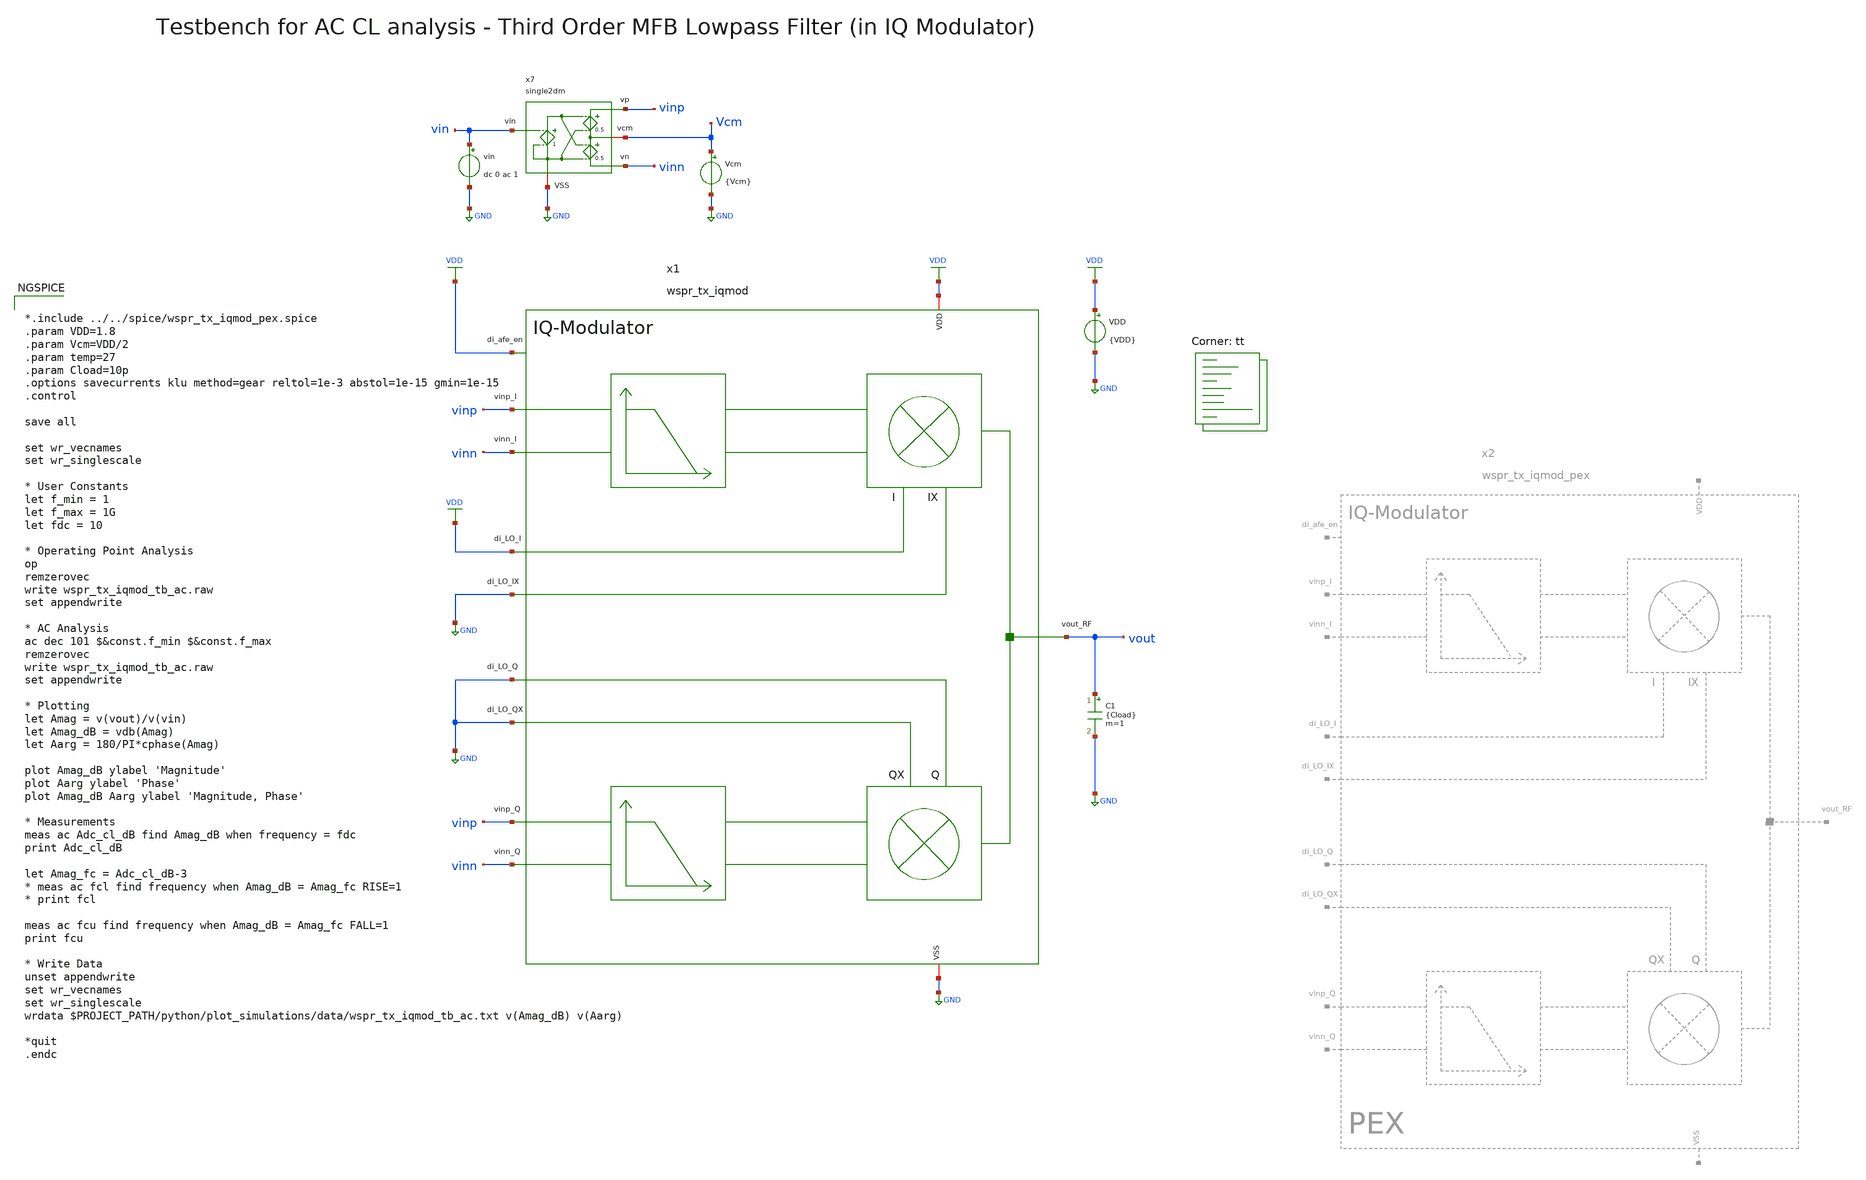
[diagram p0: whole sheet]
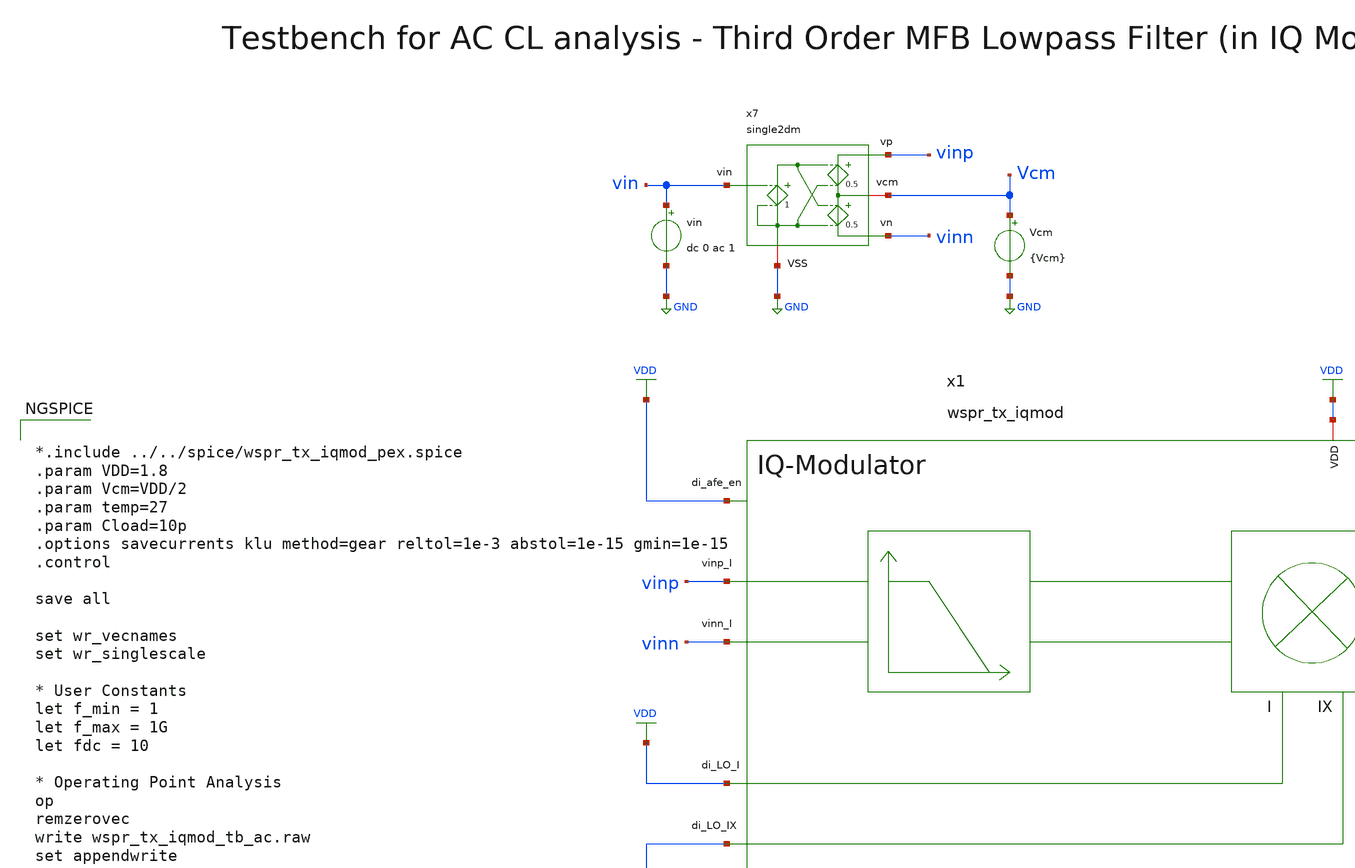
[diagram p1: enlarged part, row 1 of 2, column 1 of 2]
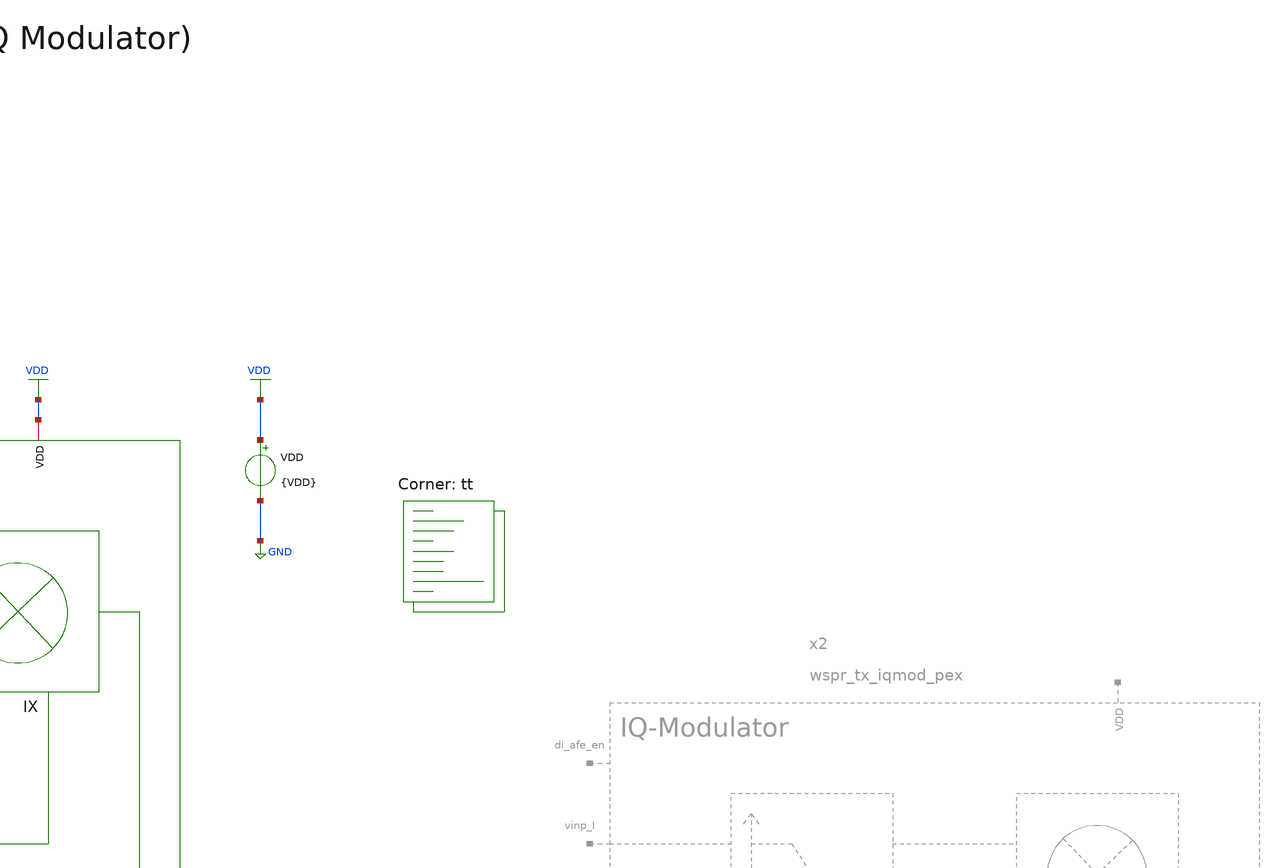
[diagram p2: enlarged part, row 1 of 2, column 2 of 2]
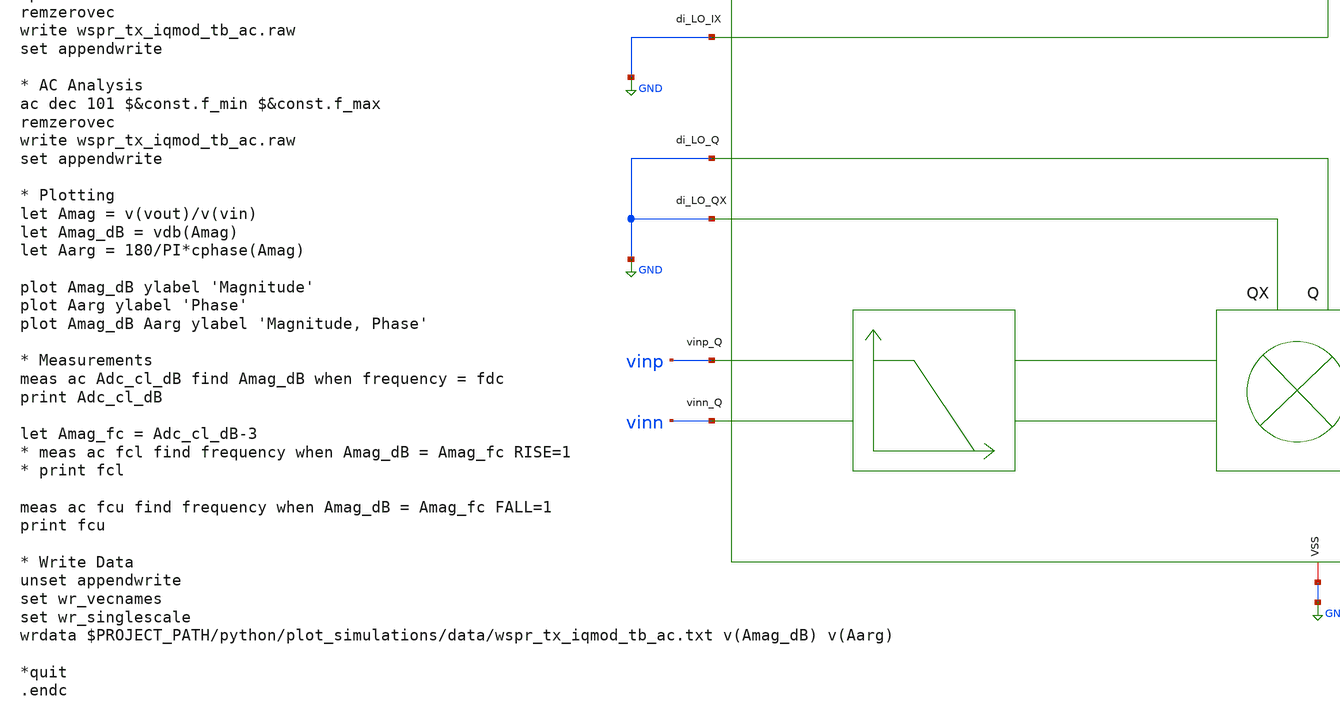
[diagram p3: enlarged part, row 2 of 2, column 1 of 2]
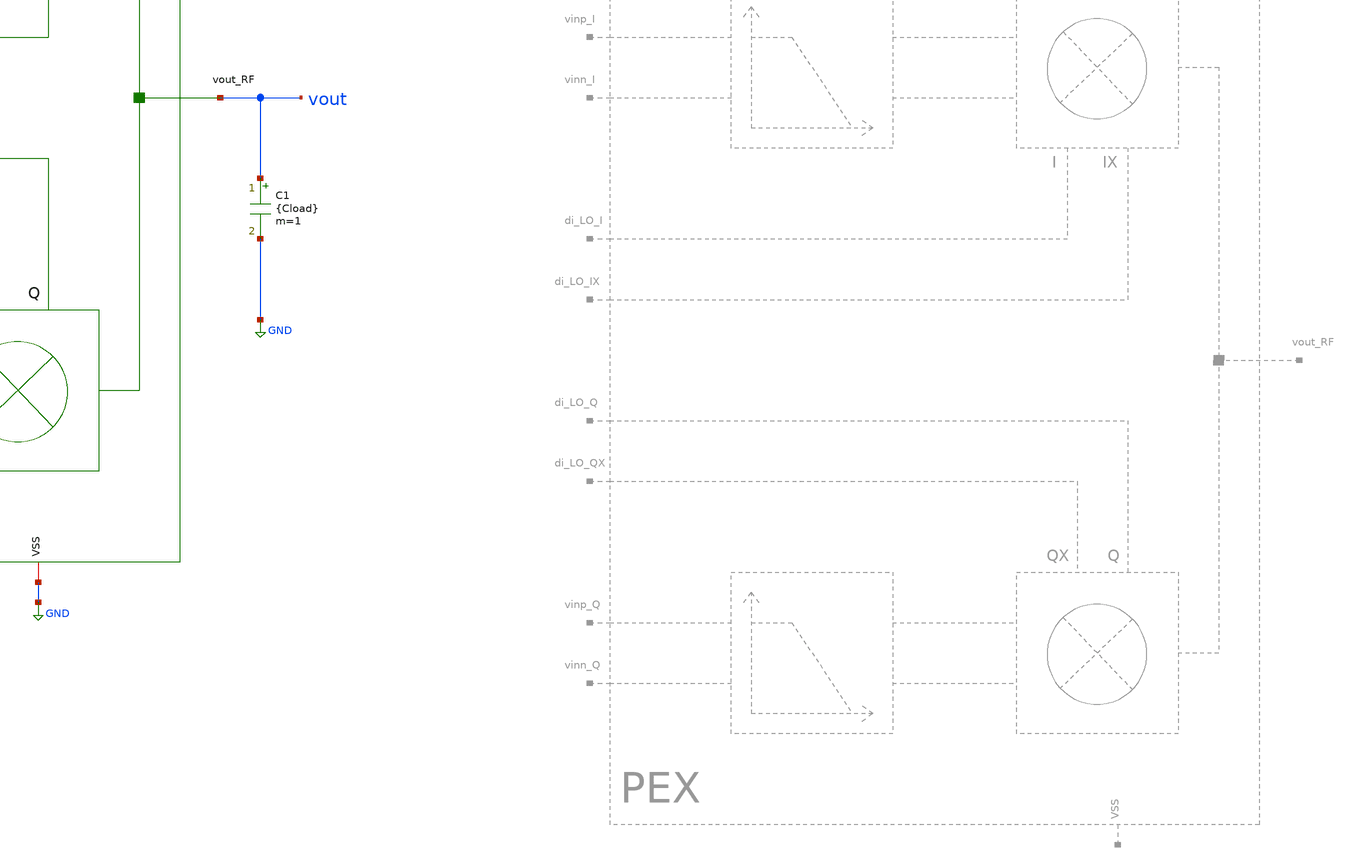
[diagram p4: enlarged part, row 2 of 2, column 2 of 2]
** sch_path: sky130/xschem/testbenches/wspr_tx_iqmod_tb_ac.sch
**.subckt wspr_tx_iqmod_tb_ac
VDD VDD GND {VDD}
C1 vout GND {Cload} m=1
x1 VDD VDD vinp vinn GND VDD GND vout vinp vinn GND GND wspr_tx_iqmod
Vcm Vcm GND {Vcm}
vin vin GND dc 0 ac 1
x7 vinp vin Vcm GND vinn single2dm
**** begin user architecture code


*.include ../../spice/wspr_tx_iqmod_pex.spice
.param VDD=1.8
.param Vcm=VDD/2
.param temp=27
.param Cload=10p
.options savecurrents klu method=gear reltol=1e-3 abstol=1e-15 gmin=1e-15
.control

save all

set wr_vecnames
set wr_singlescale

* User Constants
let f_min = 1
let f_max = 1G
let fdc = 10

* Operating Point Analysis
op
remzerovec
write wspr_tx_iqmod_tb_ac.raw
set appendwrite

* AC Analysis
ac dec 101 $&const.f_min $&const.f_max
remzerovec
write wspr_tx_iqmod_tb_ac.raw
set appendwrite

* Plotting
let Amag = v(vout)/v(vin)
let Amag_dB = vdb(Amag)
let Aarg = 180/PI*cphase(Amag)

plot Amag_dB ylabel 'Magnitude'
plot Aarg ylabel 'Phase'
plot Amag_dB Aarg ylabel 'Magnitude, Phase'

* Measurements
meas ac Adc_cl_dB find Amag_dB when frequency = fdc
print Adc_cl_dB

let Amag_fc = Adc_cl_dB-3
* meas ac fcl find frequency when Amag_dB = Amag_fc RISE=1
* print fcl

meas ac fcu find frequency when Amag_dB = Amag_fc FALL=1
print fcu

* Write Data
unset appendwrite
set wr_vecnames
set wr_singlescale
wrdata $PROJECT_PATH/python/plot_simulations/data/wspr_tx_iqmod_tb_ac.txt v(Amag_dB) v(Aarg)

*quit
.endc


.lib $::SKYWATER_MODELS/sky130.lib.spice tt
**** end user architecture code
**.ends
.GLOBAL GND
.GLOBAL VDD
.end
